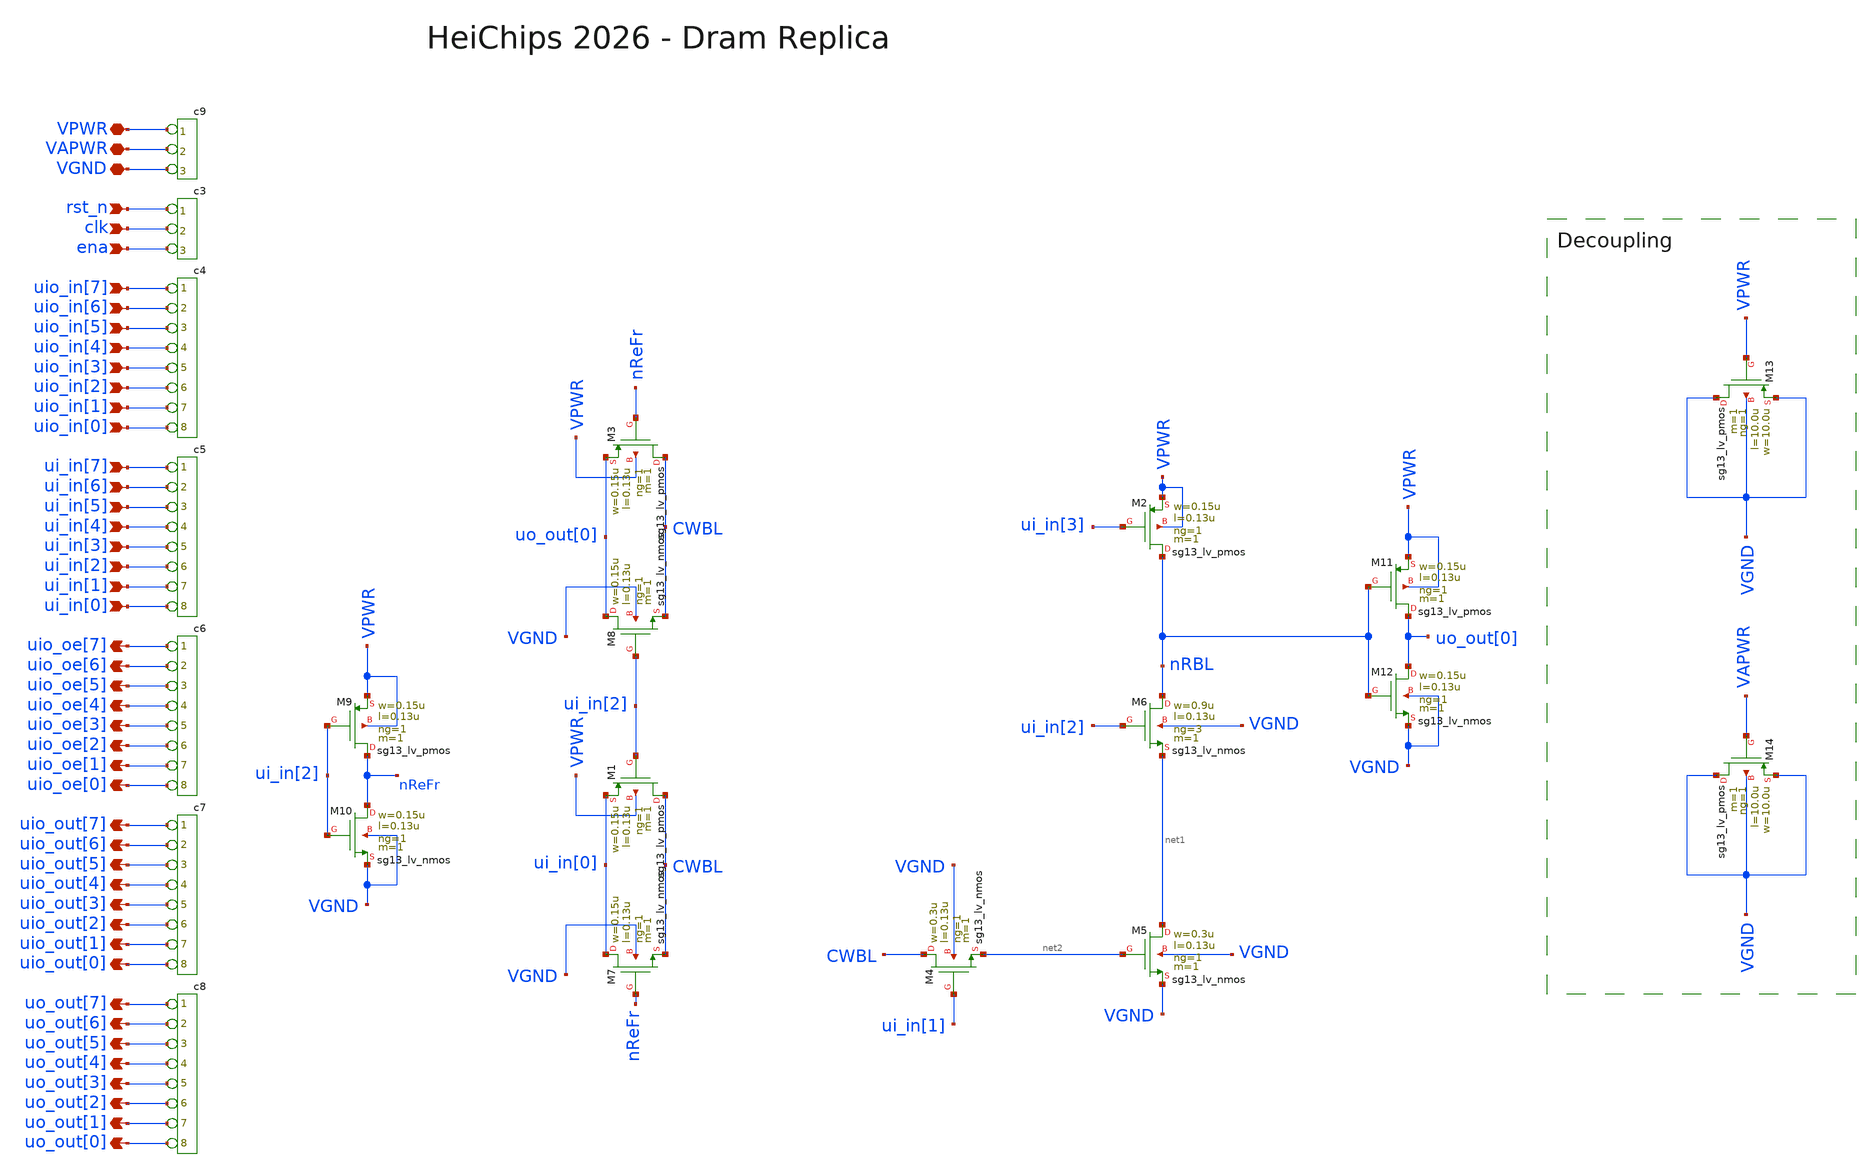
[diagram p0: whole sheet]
** sch_path: macros/heichips26_dram_replica/schematic/xschem/heichips26_dram_replica.sch
**.subckt heichips26_dram_replica rst_n clk ena uio_in[7] ui_in[7] uio_oe[7] uio_oe[6] uio_oe[5]
*+ uio_oe[4] uio_oe[3] uio_oe[2] uio_oe[1] uio_oe[0] uio_out[7] uio_out[6] uio_out[5] uio_out[4] uio_out[3]
*+ uio_out[2] uio_out[1] uio_out[0] uo_out[7] uo_out[6] uo_out[5] uo_out[4] uo_out[3] uo_out[2] uo_out[1]
*+ uo_out[0] VPWR VGND VAPWR ui_in[6] ui_in[5] ui_in[4] ui_in[3] ui_in[2] ui_in[1] ui_in[0] uio_in[6] uio_in[5]
*+ uio_in[4] uio_in[3] uio_in[2] uio_in[1] uio_in[0]
*.ipin rst_n
*.ipin clk
*.ipin ena
*.ipin uio_in[7]
*.ipin ui_in[7]
*.opin uio_oe[7]
*.opin uio_oe[6]
*.opin uio_oe[5]
*.opin uio_oe[4]
*.opin uio_oe[3]
*.opin uio_oe[2]
*.opin uio_oe[1]
*.opin uio_oe[0]
*.opin uio_out[7]
*.opin uio_out[6]
*.opin uio_out[5]
*.opin uio_out[4]
*.opin uio_out[3]
*.opin uio_out[2]
*.opin uio_out[1]
*.opin uio_out[0]
*.opin uo_out[7]
*.opin uo_out[6]
*.opin uo_out[5]
*.opin uo_out[4]
*.opin uo_out[3]
*.opin uo_out[2]
*.opin uo_out[1]
*.opin uo_out[0]
*.iopin VPWR
*.iopin VGND
*.iopin VAPWR
*.ipin ui_in[6]
*.ipin ui_in[5]
*.ipin ui_in[4]
*.ipin ui_in[3]
*.ipin ui_in[2]
*.ipin ui_in[1]
*.ipin ui_in[0]
*.ipin uio_in[6]
*.ipin uio_in[5]
*.ipin uio_in[4]
*.ipin uio_in[3]
*.ipin uio_in[2]
*.ipin uio_in[1]
*.ipin uio_in[0]
XM4 CWBL ui_in[1] net2 VGND sg13_lv_nmos w=0.3u l=0.13u ng=1 m=1 mm_ok=1
XM5 net1 net2 VGND VGND sg13_lv_nmos w=0.3u l=0.13u ng=1 m=1 mm_ok=1
XM6 nRBL ui_in[2] net1 VGND sg13_lv_nmos w=0.9u l=0.13u ng=3 m=1 mm_ok=1
XM2 nRBL ui_in[3] VPWR VPWR sg13_lv_pmos w=0.15u l=0.13u ng=1 m=1 mm_ok=1
XM1 CWBL ui_in[2] ui_in[0] VPWR sg13_lv_pmos w=0.15u l=0.13u ng=1 m=1 mm_ok=1
XM7 ui_in[0] nReFr CWBL VGND sg13_lv_nmos w=0.15u l=0.13u ng=1 m=1 mm_ok=1
XM3 CWBL nReFr uo_out[0] VPWR sg13_lv_pmos w=0.15u l=0.13u ng=1 m=1 mm_ok=1
XM8 uo_out[0] ui_in[2] CWBL VGND sg13_lv_nmos w=0.15u l=0.13u ng=1 m=1 mm_ok=1
XM9 nReFr ui_in[2] VPWR VPWR sg13_lv_pmos w=0.15u l=0.13u ng=1 m=1 mm_ok=1
XM10 nReFr ui_in[2] VGND VGND sg13_lv_nmos w=0.15u l=0.13u ng=1 m=1 mm_ok=1
XM11 uo_out[0] nRBL VPWR VPWR sg13_lv_pmos w=0.15u l=0.13u ng=1 m=1 mm_ok=1
XM12 uo_out[0] nRBL VGND VGND sg13_lv_nmos w=0.15u l=0.13u ng=1 m=1 mm_ok=1
*connector(3,1) ?1 rst_n ?1 clk ?1 ena
*connector(8,1) ?1 uio_in[7] ?1 uio_in[6] ?1 uio_in[5] ?1 uio_in[4] ?1 uio_in[3] ?1 uio_in[2] ?1
*+ uio_in[1] ?1 uio_in[0]
*connector(8,1) ?1 ui_in[7] ?1 ui_in[6] ?1 ui_in[5] ?1 ui_in[4] ?1 ui_in[3] ?1 ui_in[2] ?1 ui_in[1]
*+ ?1 ui_in[0]
*connector(8,1) ?1 uio_oe[7] ?1 uio_oe[6] ?1 uio_oe[5] ?1 uio_oe[4] ?1 uio_oe[3] ?1 uio_oe[2] ?1
*+ uio_oe[1] ?1 uio_oe[0]
*connector(8,1) ?1 uio_out[7] ?1 uio_out[6] ?1 uio_out[5] ?1 uio_out[4] ?1 uio_out[3] ?1 uio_out[2]
*+ ?1 uio_out[1] ?1 uio_out[0]
*connector(8,1) ?1 uo_out[7] ?1 uo_out[6] ?1 uo_out[5] ?1 uo_out[4] ?1 uo_out[3] ?1 uo_out[2] ?1
*+ uo_out[1] ?1 uo_out[0]
*connector(3,1) ?1 VPWR ?1 VAPWR ?1 VGND
XM13 VGND VPWR VGND VGND sg13_lv_pmos w=10.0u l=10.0u ng=1 m=1 mm_ok=1
XM14 VGND VAPWR VGND VGND sg13_lv_pmos w=10.0u l=10.0u ng=1 m=1 mm_ok=1
**.ends
.end
